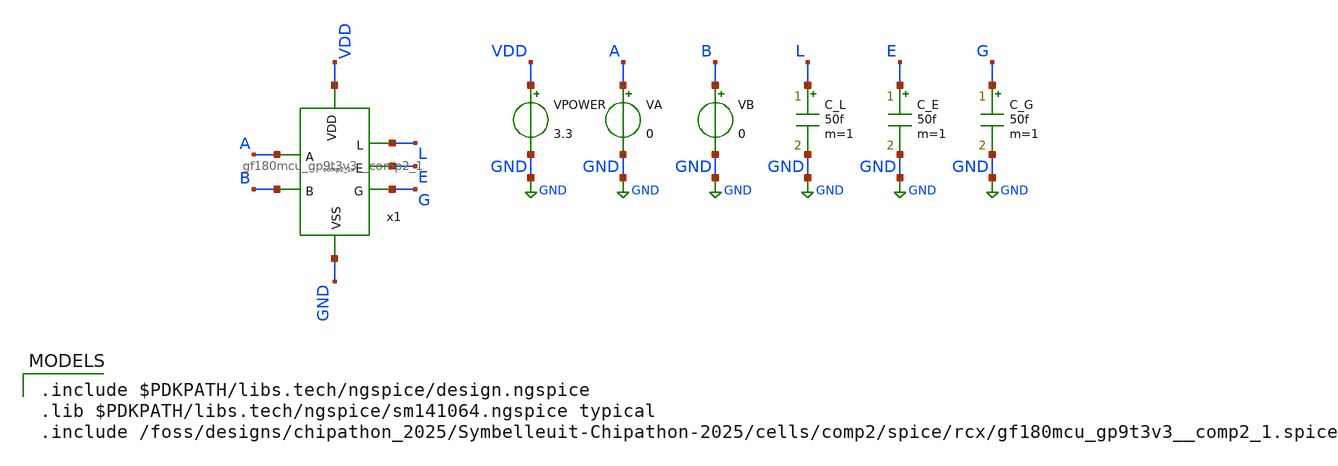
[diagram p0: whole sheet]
** sch_path: cells/comp2/cace/templates/comp2_tb_iddq.sch
**.subckt comp2_tb_iddq
x1 VDD L A E G B GND gf180mcu_gp9t3v3__comp2_1
VPOWER VDD GND 3.3
.save i(vpower)
VA A GND 0
VB B GND 0
C_L L GND 50f m=1
C_E E GND 50f m=1
C_G G GND 50f m=1
**** begin user architecture code

.include $PDKPATH/libs.tech/ngspice/design.ngspice
.lib $PDKPATH/libs.tech/ngspice/sm141064.ngspice typical
.include /foss/designs/chipathon_2025/Symbelleuit-Chipathon-2025/cells/comp2/spice/rcx/gf180mcu_gp9t3v3__comp2_1.spice


* CACE IDDQ Quiescent Leakage Simulation
.control
  dc VA 0 3.3 3.3 VB 0 3.3 3.3
  let iddq = abs(i(VPOWER))
  let iddq_max = vecmax(iddq)
  print iddq_max
  echo $&iddq_max > comp2_tb_iddq_0.data
.endc
.GLOBAL GND


**** end user architecture code
**.ends
.GLOBAL GND
.end
